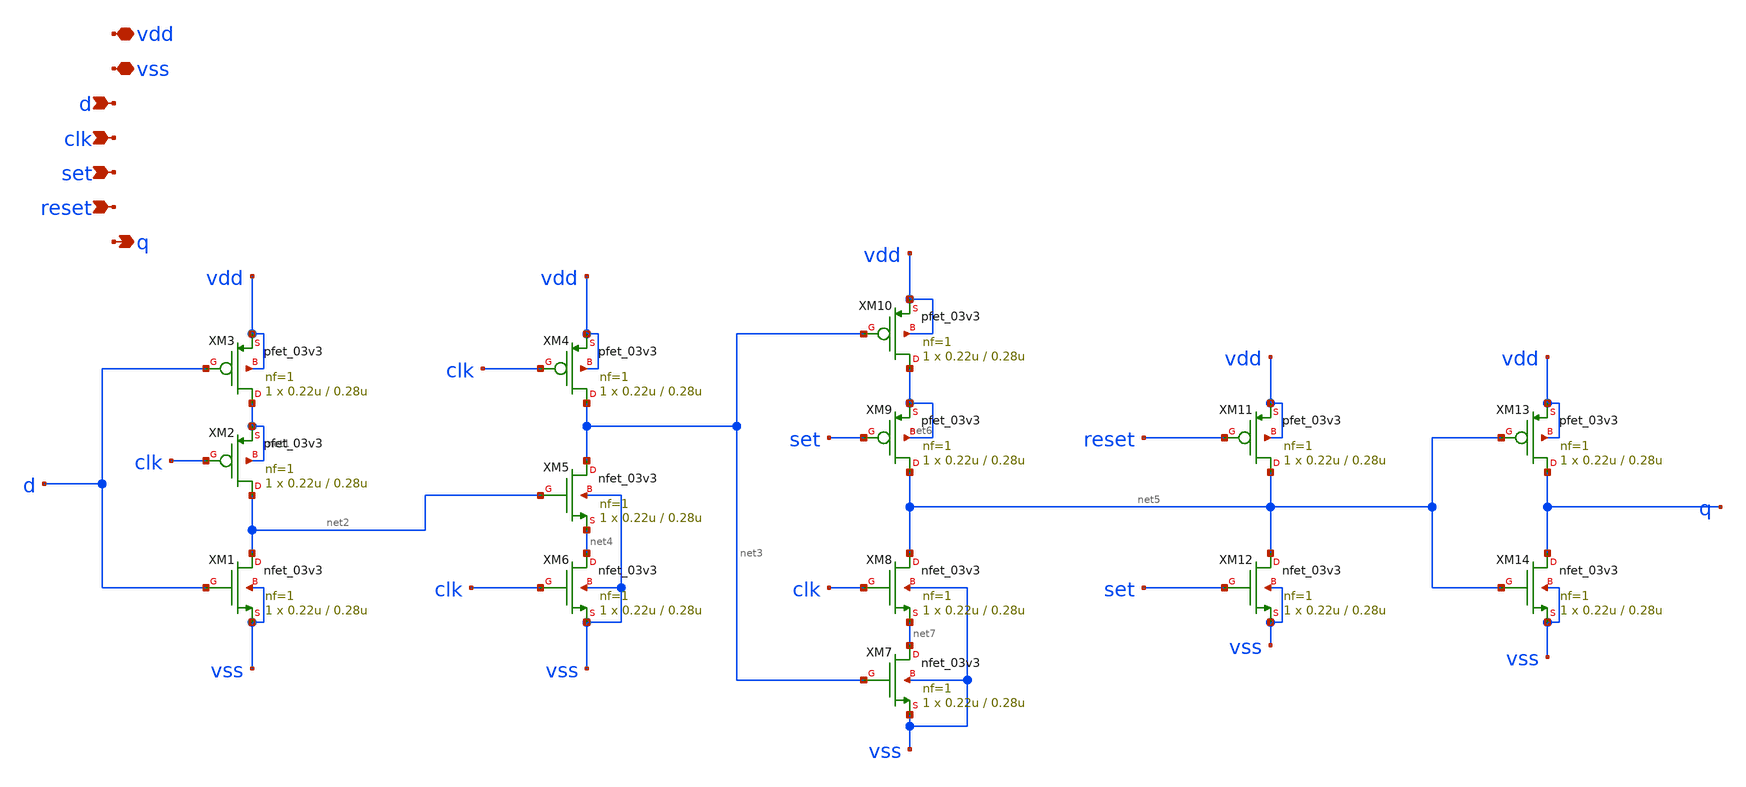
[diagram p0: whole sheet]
** sch_path: designs/libs/tspc_flip_flop/tspc_flip_flop.sch
**.subckt tspc_flip_flop vdd vss d clk set reset q
*.iopin vdd
*.iopin vss
*.ipin d
*.ipin clk
*.ipin set
*.ipin reset
*.opin q
XM1 net2 d vss vss nfet_03v3 L=0.28u W=0.22u nf=1 ad='int((nf+1)/2) * W/nf * 0.18u' as='int((nf+2)/2) * W/nf * 0.18u'
+ pd='2*int((nf+1)/2) * (W/nf + 0.18u)' ps='2*int((nf+2)/2) * (W/nf + 0.18u)' nrd='0.18u / W' nrs='0.18u / W'
+ sa=0 sb=0 sd=0 m=1
XM2 net2 clk net1 net1 pfet_03v3 L=0.28u W=0.22u nf=1 ad='int((nf+1)/2) * W/nf * 0.18u' as='int((nf+2)/2) * W/nf * 0.18u'
+ pd='2*int((nf+1)/2) * (W/nf + 0.18u)' ps='2*int((nf+2)/2) * (W/nf + 0.18u)' nrd='0.18u / W' nrs='0.18u / W'
+ sa=0 sb=0 sd=0 m=1
XM3 net1 d vdd vdd pfet_03v3 L=0.28u W=0.22u nf=1 ad='int((nf+1)/2) * W/nf * 0.18u' as='int((nf+2)/2) * W/nf * 0.18u'
+ pd='2*int((nf+1)/2) * (W/nf + 0.18u)' ps='2*int((nf+2)/2) * (W/nf + 0.18u)' nrd='0.18u / W' nrs='0.18u / W'
+ sa=0 sb=0 sd=0 m=1
XM4 net3 clk vdd vdd pfet_03v3 L=0.28u W=0.22u nf=1 ad='int((nf+1)/2) * W/nf * 0.18u' as='int((nf+2)/2) * W/nf * 0.18u'
+ pd='2*int((nf+1)/2) * (W/nf + 0.18u)' ps='2*int((nf+2)/2) * (W/nf + 0.18u)' nrd='0.18u / W' nrs='0.18u / W'
+ sa=0 sb=0 sd=0 m=1
XM5 net3 net2 net4 vss nfet_03v3 L=0.28u W=0.22u nf=1 ad='int((nf+1)/2) * W/nf * 0.18u' as='int((nf+2)/2) * W/nf * 0.18u'
+ pd='2*int((nf+1)/2) * (W/nf + 0.18u)' ps='2*int((nf+2)/2) * (W/nf + 0.18u)' nrd='0.18u / W' nrs='0.18u / W'
+ sa=0 sb=0 sd=0 m=1
XM6 net4 clk vss vss nfet_03v3 L=0.28u W=0.22u nf=1 ad='int((nf+1)/2) * W/nf * 0.18u' as='int((nf+2)/2) * W/nf * 0.18u'
+ pd='2*int((nf+1)/2) * (W/nf + 0.18u)' ps='2*int((nf+2)/2) * (W/nf + 0.18u)' nrd='0.18u / W' nrs='0.18u / W'
+ sa=0 sb=0 sd=0 m=1
XM7 net7 net3 vss vss nfet_03v3 L=0.28u W=0.22u nf=1 ad='int((nf+1)/2) * W/nf * 0.18u' as='int((nf+2)/2) * W/nf * 0.18u'
+ pd='2*int((nf+1)/2) * (W/nf + 0.18u)' ps='2*int((nf+2)/2) * (W/nf + 0.18u)' nrd='0.18u / W' nrs='0.18u / W'
+ sa=0 sb=0 sd=0 m=1
XM8 net5 clk net7 vss nfet_03v3 L=0.28u W=0.22u nf=1 ad='int((nf+1)/2) * W/nf * 0.18u' as='int((nf+2)/2) * W/nf * 0.18u'
+ pd='2*int((nf+1)/2) * (W/nf + 0.18u)' ps='2*int((nf+2)/2) * (W/nf + 0.18u)' nrd='0.18u / W' nrs='0.18u / W'
+ sa=0 sb=0 sd=0 m=1
XM9 net5 set net6 net6 pfet_03v3 L=0.28u W=0.22u nf=1 ad='int((nf+1)/2) * W/nf * 0.18u' as='int((nf+2)/2) * W/nf * 0.18u'
+ pd='2*int((nf+1)/2) * (W/nf + 0.18u)' ps='2*int((nf+2)/2) * (W/nf + 0.18u)' nrd='0.18u / W' nrs='0.18u / W'
+ sa=0 sb=0 sd=0 m=1
XM10 net6 net3 vdd vdd pfet_03v3 L=0.28u W=0.22u nf=1 ad='int((nf+1)/2) * W/nf * 0.18u' as='int((nf+2)/2) * W/nf * 0.18u'
+ pd='2*int((nf+1)/2) * (W/nf + 0.18u)' ps='2*int((nf+2)/2) * (W/nf + 0.18u)' nrd='0.18u / W' nrs='0.18u / W'
+ sa=0 sb=0 sd=0 m=1
XM11 net5 reset vdd vdd pfet_03v3 L=0.28u W=0.22u nf=1 ad='int((nf+1)/2) * W/nf * 0.18u' as='int((nf+2)/2) * W/nf * 0.18u'
+ pd='2*int((nf+1)/2) * (W/nf + 0.18u)' ps='2*int((nf+2)/2) * (W/nf + 0.18u)' nrd='0.18u / W' nrs='0.18u / W'
+ sa=0 sb=0 sd=0 m=1
XM12 net5 set vss vss nfet_03v3 L=0.28u W=0.22u nf=1 ad='int((nf+1)/2) * W/nf * 0.18u' as='int((nf+2)/2) * W/nf * 0.18u'
+ pd='2*int((nf+1)/2) * (W/nf + 0.18u)' ps='2*int((nf+2)/2) * (W/nf + 0.18u)' nrd='0.18u / W' nrs='0.18u / W'
+ sa=0 sb=0 sd=0 m=1
XM13 q net5 vdd vdd pfet_03v3 L=0.28u W=0.22u nf=1 ad='int((nf+1)/2) * W/nf * 0.18u' as='int((nf+2)/2) * W/nf * 0.18u'
+ pd='2*int((nf+1)/2) * (W/nf + 0.18u)' ps='2*int((nf+2)/2) * (W/nf + 0.18u)' nrd='0.18u / W' nrs='0.18u / W'
+ sa=0 sb=0 sd=0 m=1
XM14 q net5 vss vss nfet_03v3 L=0.28u W=0.22u nf=1 ad='int((nf+1)/2) * W/nf * 0.18u' as='int((nf+2)/2) * W/nf * 0.18u'
+ pd='2*int((nf+1)/2) * (W/nf + 0.18u)' ps='2*int((nf+2)/2) * (W/nf + 0.18u)' nrd='0.18u / W' nrs='0.18u / W'
+ sa=0 sb=0 sd=0 m=1
**.ends
.end
